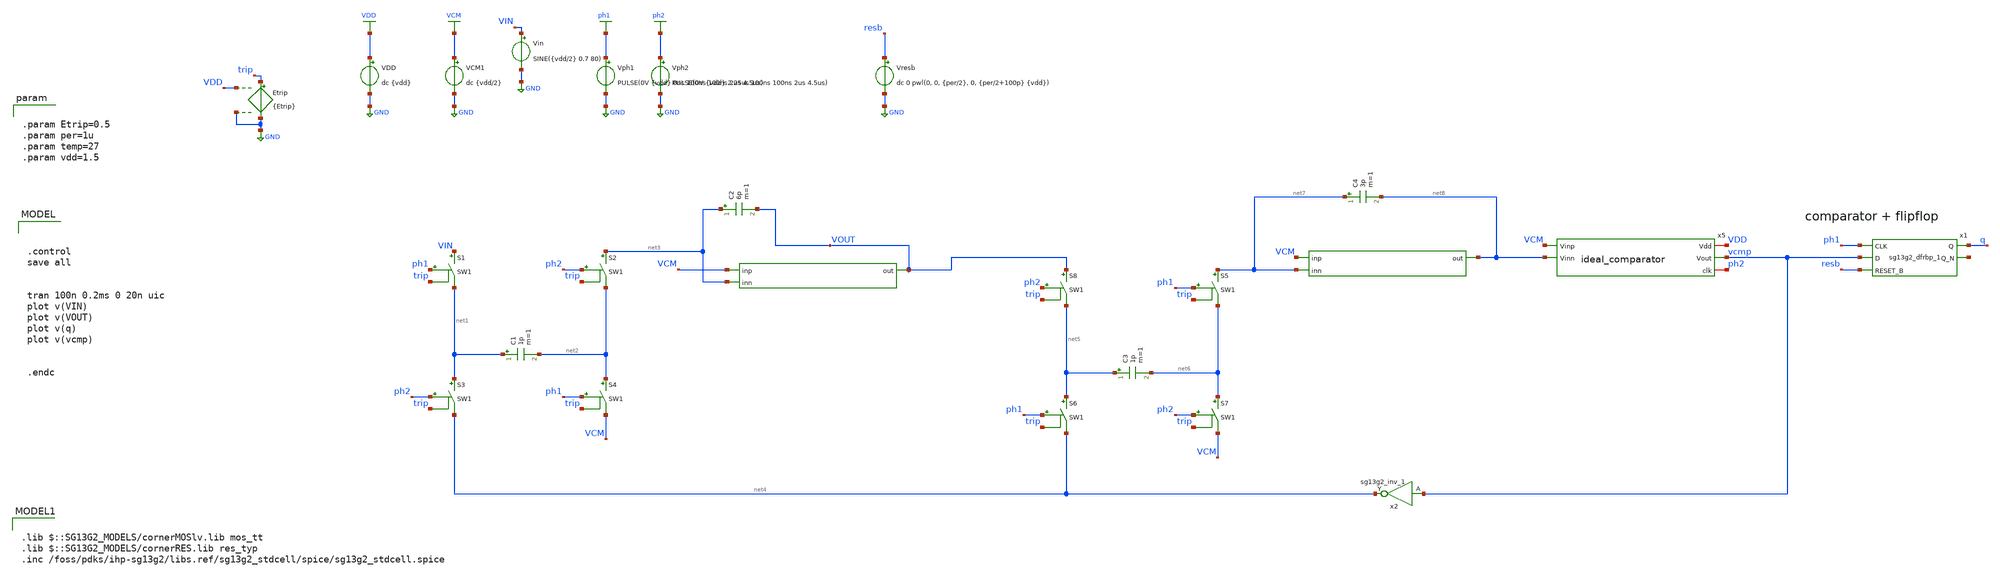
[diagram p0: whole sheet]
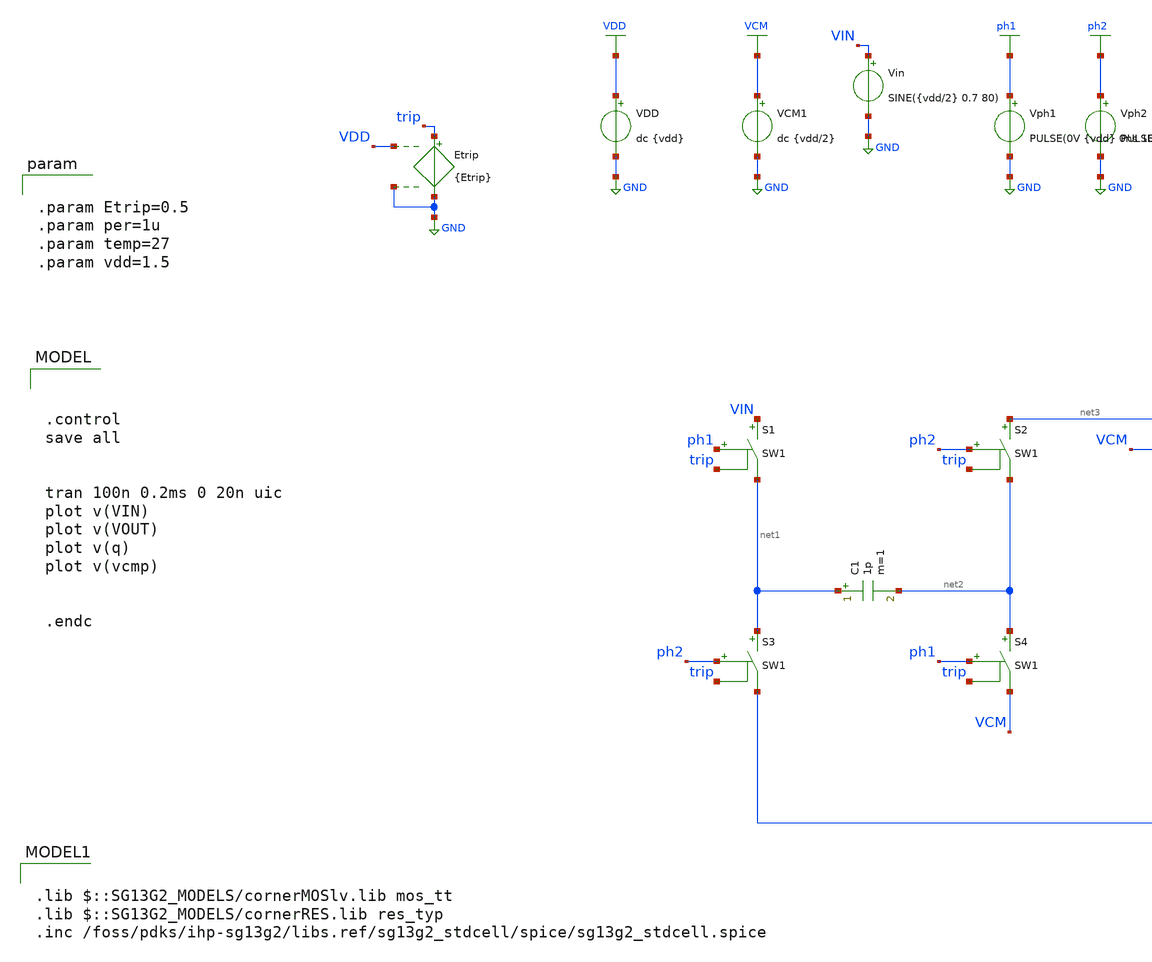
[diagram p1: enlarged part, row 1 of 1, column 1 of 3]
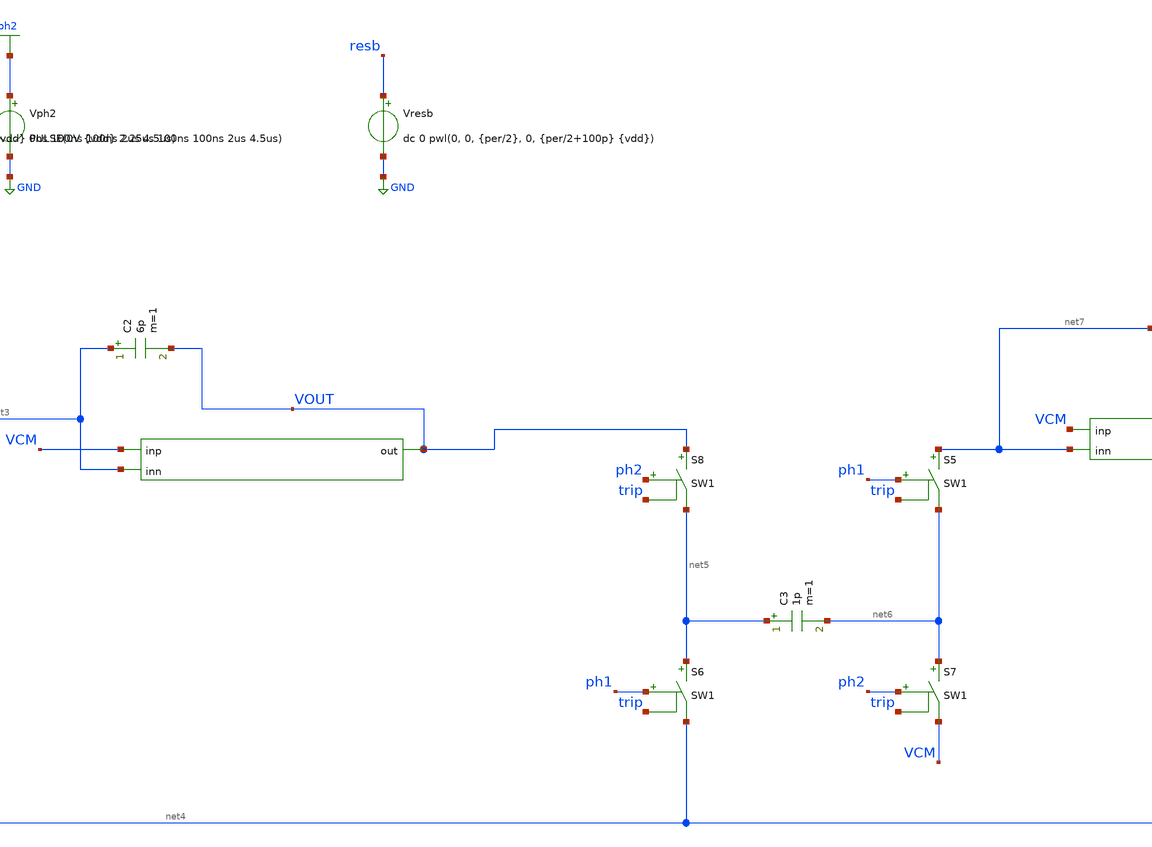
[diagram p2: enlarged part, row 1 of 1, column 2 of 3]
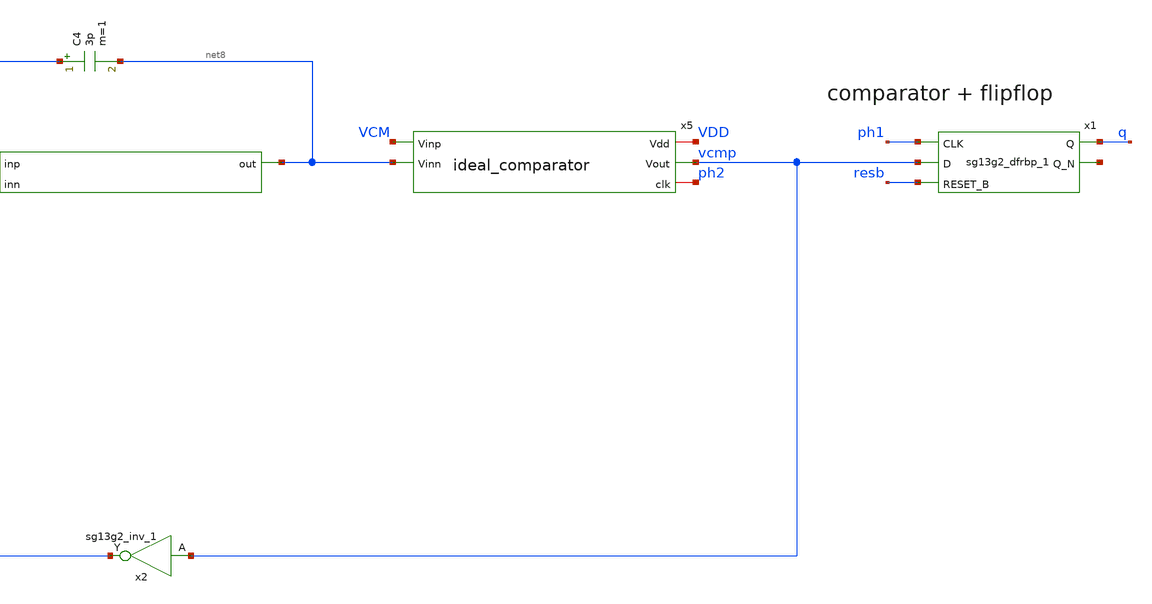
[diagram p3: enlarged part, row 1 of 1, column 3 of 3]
** sch_path: DSM_2ndOrder/1_Schematics/Ideal_Schematic/xschem/idealDSM_2ndOrder.sch
**.subckt idealDSM_2ndOrder
C1 net1 net2 1p m=1
S2 net3 net2 ph2 trip SW1
S3 net1 net4 ph2 trip SW1
S4 net2 VCM ph1 trip SW1
VDD VDD GND dc {vdd}
VCM1 VCM GND dc {vdd/2}
Vph2 ph2 GND PULSE(0V {vdd} 2.25us 100ns 100ns 2us 4.5us)
Vph1 ph1 GND PULSE(0V {vdd} 0ns 100ns 100ns 2us 4.5us)
C2 net3 VOUT 6p m=1
x1 q net9 ph1 vcmp resb 1.5 0 sg13g2_dfrbp_1
Vresb resb GND dc 0 pwl(0, 0, {per/2}, 0, {per/2+100p} {vdd})
x2 net4 vcmp 1.5 0 sg13g2_inv_1
S1 VIN net1 ph1 trip SW1
Etrip trip GND VDD GND {Etrip}
Vin VIN GND SINE({vdd/2} 0.7 80)
C3 net5 net6 1p m=1
S5 net7 net6 ph1 trip SW1
S6 net5 net4 ph1 trip SW1
S7 net6 VCM ph2 trip SW1
S8 VOUT net5 ph2 trip SW1
C4 net7 net8 3p m=1
x3 VOUT VCM net3 ideal_opamp
x4 net8 VCM net7 ideal_opamp
x5 VDD vcmp VCM ph2 net8 ideal_comparator
**** begin user architecture code



.control
save all


tran 100n 0.2ms 0 20n uic
plot v(VIN)
plot v(VOUT)
plot v(q)
plot v(vcmp)


.endc



.lib $::SG13G2_MODELS/cornerMOSlv.lib mos_tt
.lib $::SG13G2_MODELS/cornerRES.lib res_typ
.inc /foss/pdks/ihp-sg13g2/libs.ref/sg13g2_stdcell/spice/sg13g2_stdcell.spice



.param Etrip=0.5
.param per=1u
.param temp=27
.param vdd=1.5


**** end user architecture code
**.ends
.GLOBAL GND
.GLOBAL VDD
.GLOBAL VCM
.GLOBAL ph2
.GLOBAL ph1
**** begin user architecture code
.MODEL SW1 SW(VT=0.1 VH=0 RON=0.1 ROFF=100M)
**** end user architecture code
.end
